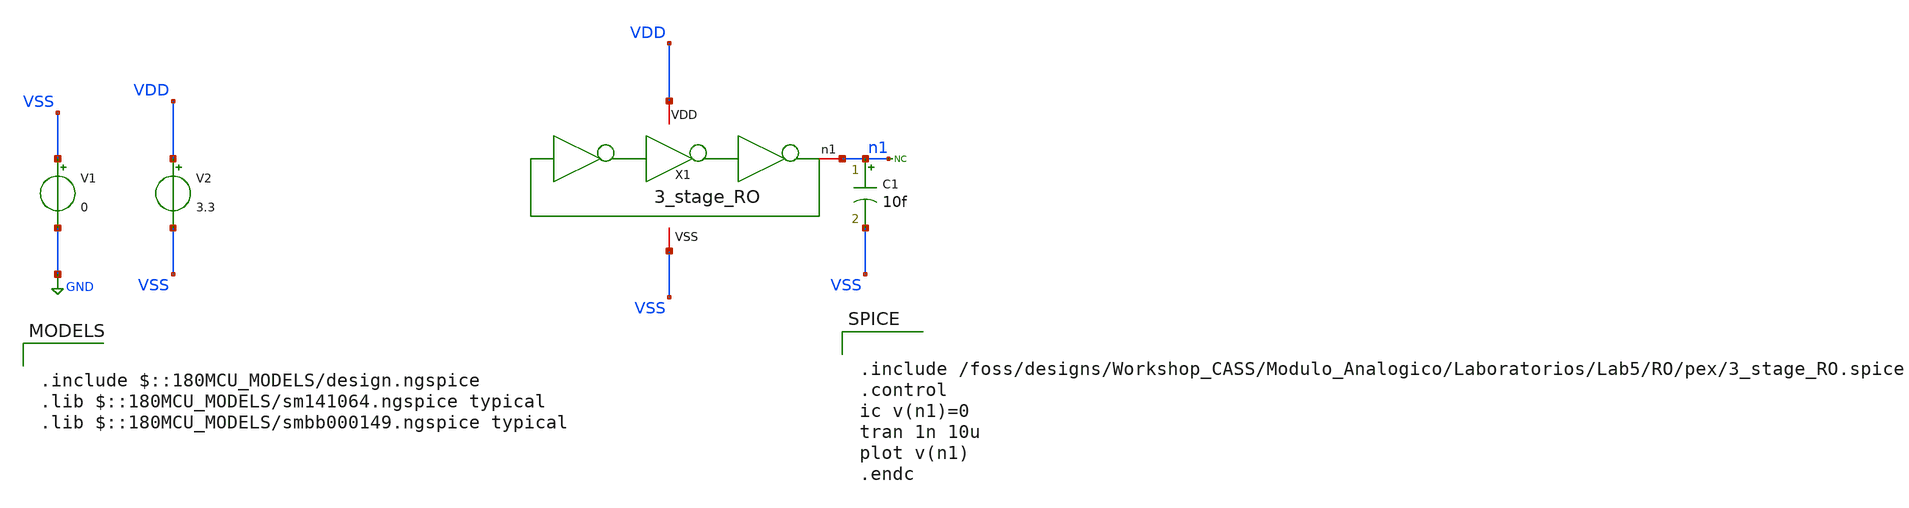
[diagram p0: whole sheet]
** sch_path: gf180_examples/RO/pex/3_stage_RO_tb_tran.sch
**.subckt 3_stage_RO_tb_tran
V1 VSS GND 0
V2 VDD VSS 3.3
* noconn n1
X1 VDD VSS n1 3_stage_RO
C1 n1 VSS 10f m=1
**** begin user architecture code

.include $::180MCU_MODELS/design.ngspice
.lib $::180MCU_MODELS/sm141064.ngspice typical
.lib $::180MCU_MODELS/smbb000149.ngspice typical



.include /foss/designs/Workshop_CASS/Modulo_Analogico/Laboratorios/Lab5/RO/pex/3_stage_RO.spice
.control
ic v(n1)=0
tran 1n 10u
plot v(n1)
.endc


**** end user architecture code
**.ends
.GLOBAL GND
.end
